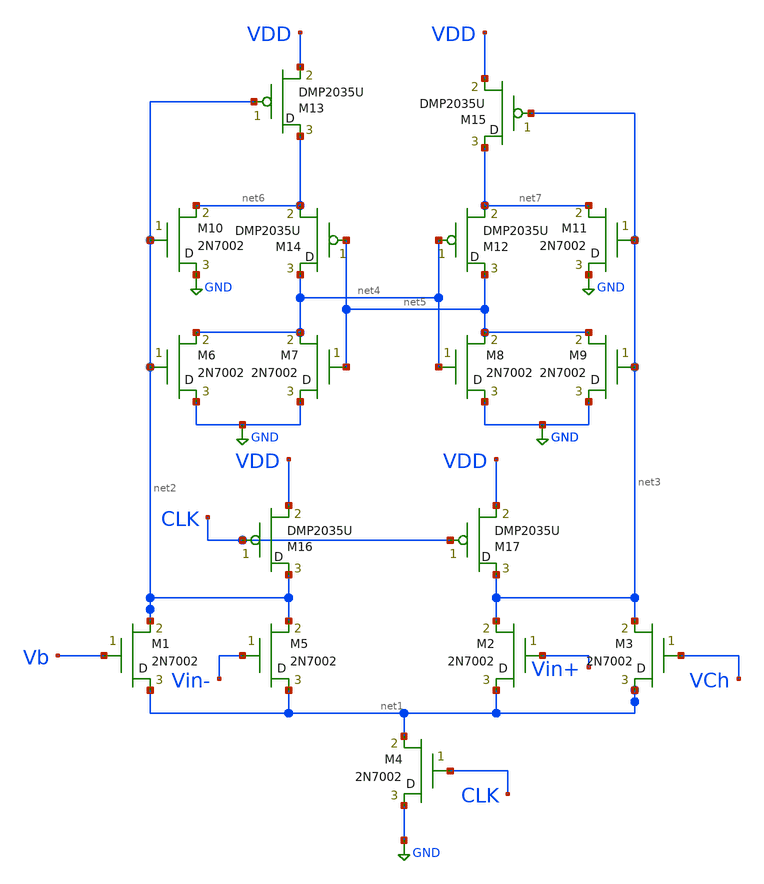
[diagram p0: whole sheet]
** sch_path: ISSCC25/accepted_notebooks/MicroNina/sch/Miyahara.sch
**.subckt Miyahara
M2 net1 Vin+ net3 M2N7002 m=1
M4 GND CLK net1 M2N7002 m=1
M5 net1 Vin- net2 M2N7002 m=1
M1 net1 Vb net2 M2N7002 m=1
M3 net1 VCh net3 M2N7002 m=1
M6 GND net2 net4 M2N7002 m=1
M7 GND net5 net4 M2N7002 m=1
M8 GND net4 net5 M2N7002 m=1
M9 GND net3 net5 M2N7002 m=1
M10 GND net2 net6 M2N7002 m=1
M11 GND net3 net7 M2N7002 m=1
M12 net5 net4 net7 DMP2035U m=1
M13 net6 net2 VDD DMP2035U m=1
M14 net4 net5 net6 DMP2035U m=1
M15 net7 net3 VDD DMP2035U m=1
M16 net2 CLK VDD DMP2035U m=1
M17 net3 CLK VDD DMP2035U m=1
**.ends
.GLOBAL GND
.end
